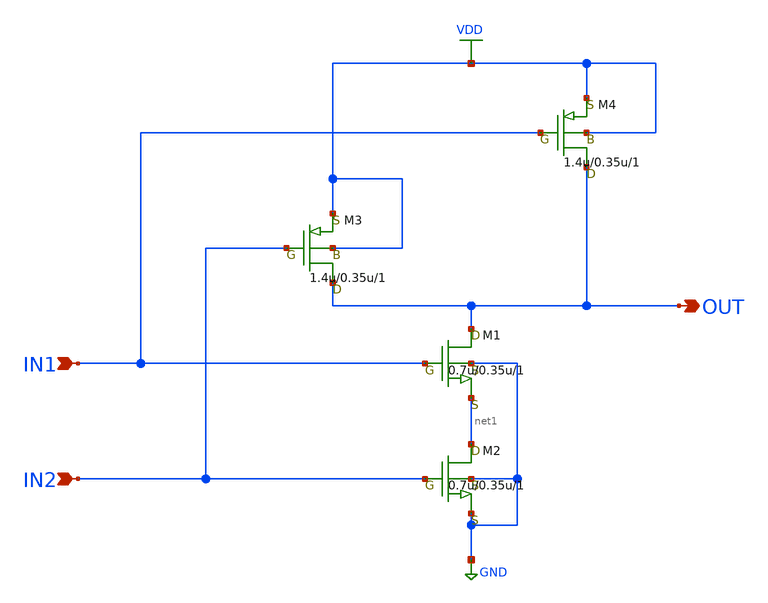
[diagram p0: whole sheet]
** sch_path: LR_hokari/LR_Work2/Clocked_Comparator_Xschem/NAND2.sch
**.subckt NAND2 IN1 OUT IN2
*.ipin IN1
*.opin OUT
*.ipin IN2
M1 OUT IN1 net1 GND nch w=0.7u l=0.35u as=0.56p ps=3u ad=0.56p pd=3u m=1
M3 OUT IN2 VDD VDD pch w=1.4u l=0.35u as=1.2p ps=4.6u ad=1.2p pd=4.6u m=1
M4 OUT IN1 VDD VDD pch w=1.4u l=0.35u as=1.2p ps=4.6u ad=1.2p pd=4.6u m=1
M2 net1 IN2 GND GND nch w=0.7u l=0.35u as=0.56p ps=3u ad=0.56p pd=3u m=1
**.ends
.GLOBAL GND
.GLOBAL VDD
.end
